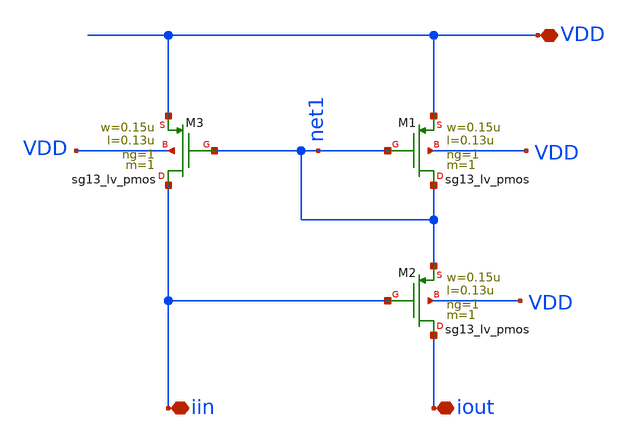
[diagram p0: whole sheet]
** sch_path: analog-db/templates/current_mirror/pmos_current_source/wilson_current_mirror.sch
**.subckt wilson_current_mirror VDD iin iout
*.iopin VDD
*.iopin iin
*.iopin iout
XM1 net1 net1 VDD VDD sg13_lv_pmos w=0.15u l=0.13u ng=1 m=1 mm_ok=1
XM2 iout iin net1 VDD sg13_lv_pmos w=0.15u l=0.13u ng=1 m=1 mm_ok=1
XM3 iin net1 VDD VDD sg13_lv_pmos w=0.15u l=0.13u ng=1 m=1 mm_ok=1
**.ends
.end
